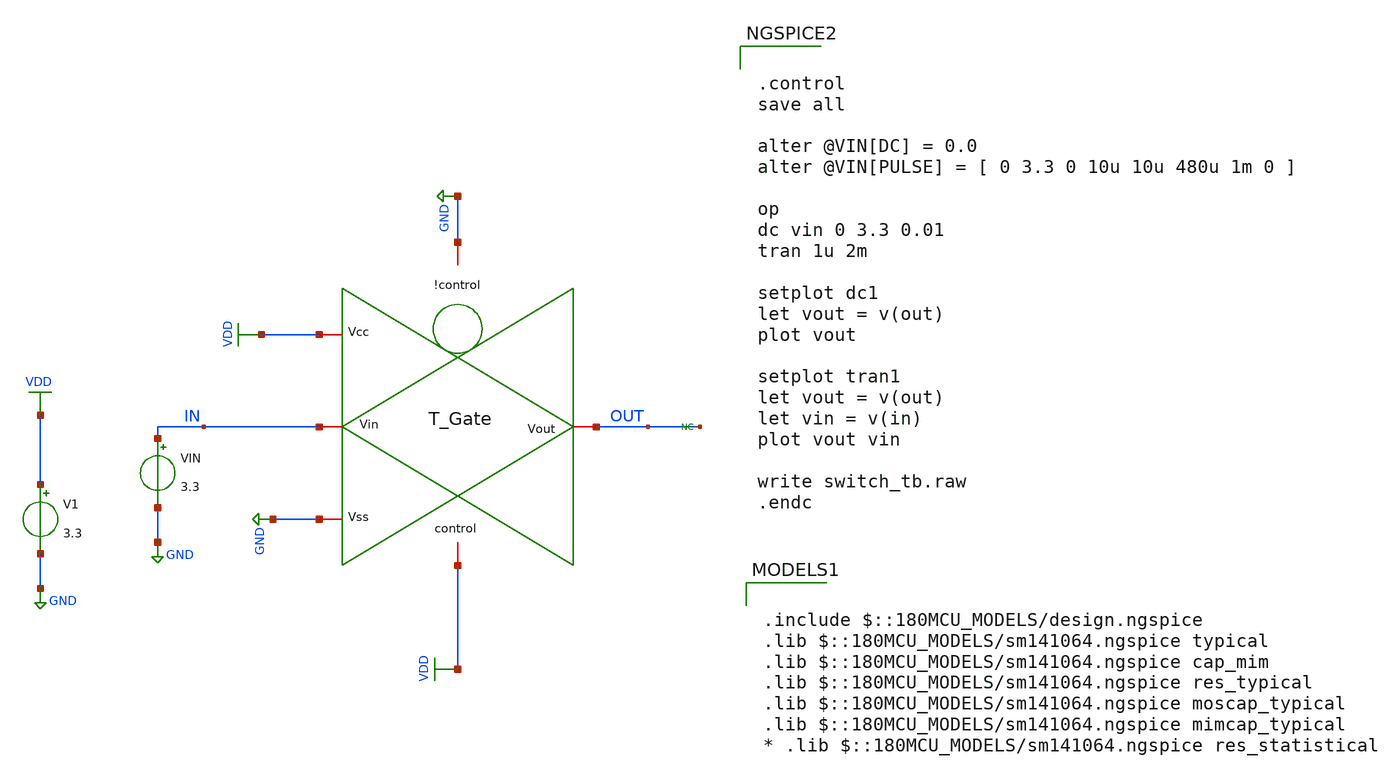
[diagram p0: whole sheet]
** sch_path: Array Components/Switch Array/T Gate/T_gate_1_tb.sch
**.subckt T_gate_1_tb
V1 VDD GND 3.3
x2 GND VDD IN OUT GND VDD T_gate
VIN IN GND 3.3
* noconn OUT
**** begin user architecture code

.include $::180MCU_MODELS/design.ngspice
.lib $::180MCU_MODELS/sm141064.ngspice typical
.lib $::180MCU_MODELS/sm141064.ngspice cap_mim
.lib $::180MCU_MODELS/sm141064.ngspice res_typical
.lib $::180MCU_MODELS/sm141064.ngspice moscap_typical
.lib $::180MCU_MODELS/sm141064.ngspice mimcap_typical
* .lib $::180MCU_MODELS/sm141064.ngspice res_statistical



.control
save all

alter @VIN[DC] = 0.0
alter @VIN[PULSE] = [ 0 3.3 0 10u 10u 480u 1m 0 ]

op
dc vin 0 3.3 0.01
tran 1u 2m

setplot dc1
let vout = v(out)
plot vout

setplot tran1
let vout = v(out)
let vin = v(in)
plot vout vin

write switch_tb.raw
.endc


**** end user architecture code
**.ends

* expanding   symbol:  SAR ADC project/T_gate.sym # of pins=6
** sym_path: Array Components/Switch Array/T Gate/T_gate.sym
** sch_path: Array Components/Switch Array/T Gate/T_gate.sch
.subckt T_gate !control Vcc Vin Vout Vss control
*.iopin Vout
*.iopin Vin
*.iopin !control
*.iopin control
*.iopin Vss
*.iopin Vcc
XM1 Vin control Vout Vss nfet_03v3 L=0.36u W=10u nf=1 ad='int((nf+1)/2) * W/nf * 0.18u' as='int((nf+2)/2) * W/nf * 0.18u'
+ pd='2*int((nf+1)/2) * (W/nf + 0.18u)' ps='2*int((nf+2)/2) * (W/nf + 0.18u)' nrd='0.18u / W' nrs='0.18u / W'
+ sa=0 sb=0 sd=0 m=1
XM2 Vin !control Vout Vcc pfet_03v3 L=0.36u W=35u nf=1 ad='int((nf+1)/2) * W/nf * 0.18u' as='int((nf+2)/2) * W/nf * 0.18u'
+ pd='2*int((nf+1)/2) * (W/nf + 0.18u)' ps='2*int((nf+2)/2) * (W/nf + 0.18u)' nrd='0.18u / W' nrs='0.18u / W'
+ sa=0 sb=0 sd=0 m=1
.ends

.GLOBAL VDD
.GLOBAL GND
.end
